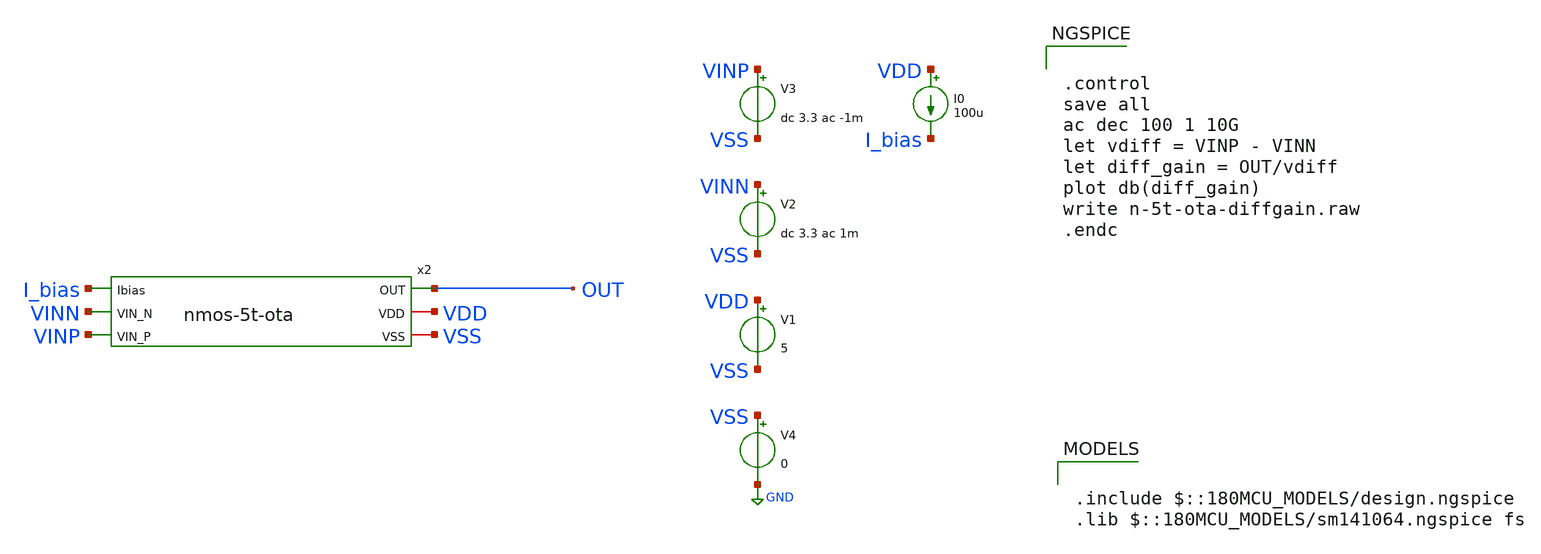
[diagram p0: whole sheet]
** sch_path: nmos-ota/nmos-5t-ota-tb.sch
**.subckt nmos-5t-ota-tb
V1 VDD VSS 5
V2 VINN VSS dc 3.3 ac 1m
V3 VINP VSS dc 3.3 ac -1m
V4 VSS GND 0
I0 VDD I_bias 100u
x2 I_bias VINN VINP OUT VDD VSS nmos-5t-ota
**** begin user architecture code

.include $::180MCU_MODELS/design.ngspice
.lib $::180MCU_MODELS/sm141064.ngspice fs



.control
save all
ac dec 100 1 10G
let vdiff = VINP - VINN
let diff_gain = OUT/vdiff
plot db(diff_gain)
write n-5t-ota-diffgain.raw
.endc


**** end user architecture code
**.ends

* expanding   symbol:  nmos-5t-ota.sym # of pins=6
** sym_path: nmos-ota/nmos-5t-ota.sym
** sch_path: nmos-ota/nmos-5t-ota.sch
.subckt nmos-5t-ota Ibias VIN_N VIN_P OUT VDD VSS
*.ipin VIN_N
*.ipin VIN_P
*.opin OUT
*.iopin VDD
*.iopin VSS
*.ipin Ibias
XM1 net2 net2 VDD VDD pfet_03v3 L=1.5u W=25u nf=1 ad='int((nf+1)/2) * W/nf * 0.18u' as='int((nf+2)/2) * W/nf * 0.18u'
+ pd='2*int((nf+1)/2) * (W/nf + 0.18u)' ps='2*int((nf+2)/2) * (W/nf + 0.18u)' nrd='0.18u / W' nrs='0.18u / W'
+ sa=0 sb=0 sd=0 m=1
XM2 OUT net2 VDD VDD pfet_03v3 L=1.5u W=25u nf=1 ad='int((nf+1)/2) * W/nf * 0.18u' as='int((nf+2)/2) * W/nf * 0.18u'
+ pd='2*int((nf+1)/2) * (W/nf + 0.18u)' ps='2*int((nf+2)/2) * (W/nf + 0.18u)' nrd='0.18u / W' nrs='0.18u / W'
+ sa=0 sb=0 sd=0 m=1
XM3 OUT VIN_N net1 net1 nfet_03v3 L=1.5u W=16.5u nf=1 ad='int((nf+1)/2) * W/nf * 0.18u' as='int((nf+2)/2) * W/nf * 0.18u'
+ pd='2*int((nf+1)/2) * (W/nf + 0.18u)' ps='2*int((nf+2)/2) * (W/nf + 0.18u)' nrd='0.18u / W' nrs='0.18u / W'
+ sa=0 sb=0 sd=0 m=1
XM4 net2 VIN_P net1 net1 nfet_03v3 L=1.5u W=16.5u nf=1 ad='int((nf+1)/2) * W/nf * 0.18u' as='int((nf+2)/2) * W/nf * 0.18u'
+ pd='2*int((nf+1)/2) * (W/nf + 0.18u)' ps='2*int((nf+2)/2) * (W/nf + 0.18u)' nrd='0.18u / W' nrs='0.18u / W'
+ sa=0 sb=0 sd=0 m=1
XM5 Ibias Ibias VSS VSS nfet_03v3 L=2u W=12.5u nf=1 ad='int((nf+1)/2) * W/nf * 0.18u' as='int((nf+2)/2) * W/nf * 0.18u'
+ pd='2*int((nf+1)/2) * (W/nf + 0.18u)' ps='2*int((nf+2)/2) * (W/nf + 0.18u)' nrd='0.18u / W' nrs='0.18u / W'
+ sa=0 sb=0 sd=0 m=1
XM6 net1 Ibias VSS VSS nfet_03v3 L=2u W=25u nf=1 ad='int((nf+1)/2) * W/nf * 0.18u' as='int((nf+2)/2) * W/nf * 0.18u'
+ pd='2*int((nf+1)/2) * (W/nf + 0.18u)' ps='2*int((nf+2)/2) * (W/nf + 0.18u)' nrd='0.18u / W' nrs='0.18u / W'
+ sa=0 sb=0 sd=0 m=1
.ends

.GLOBAL GND
.end
